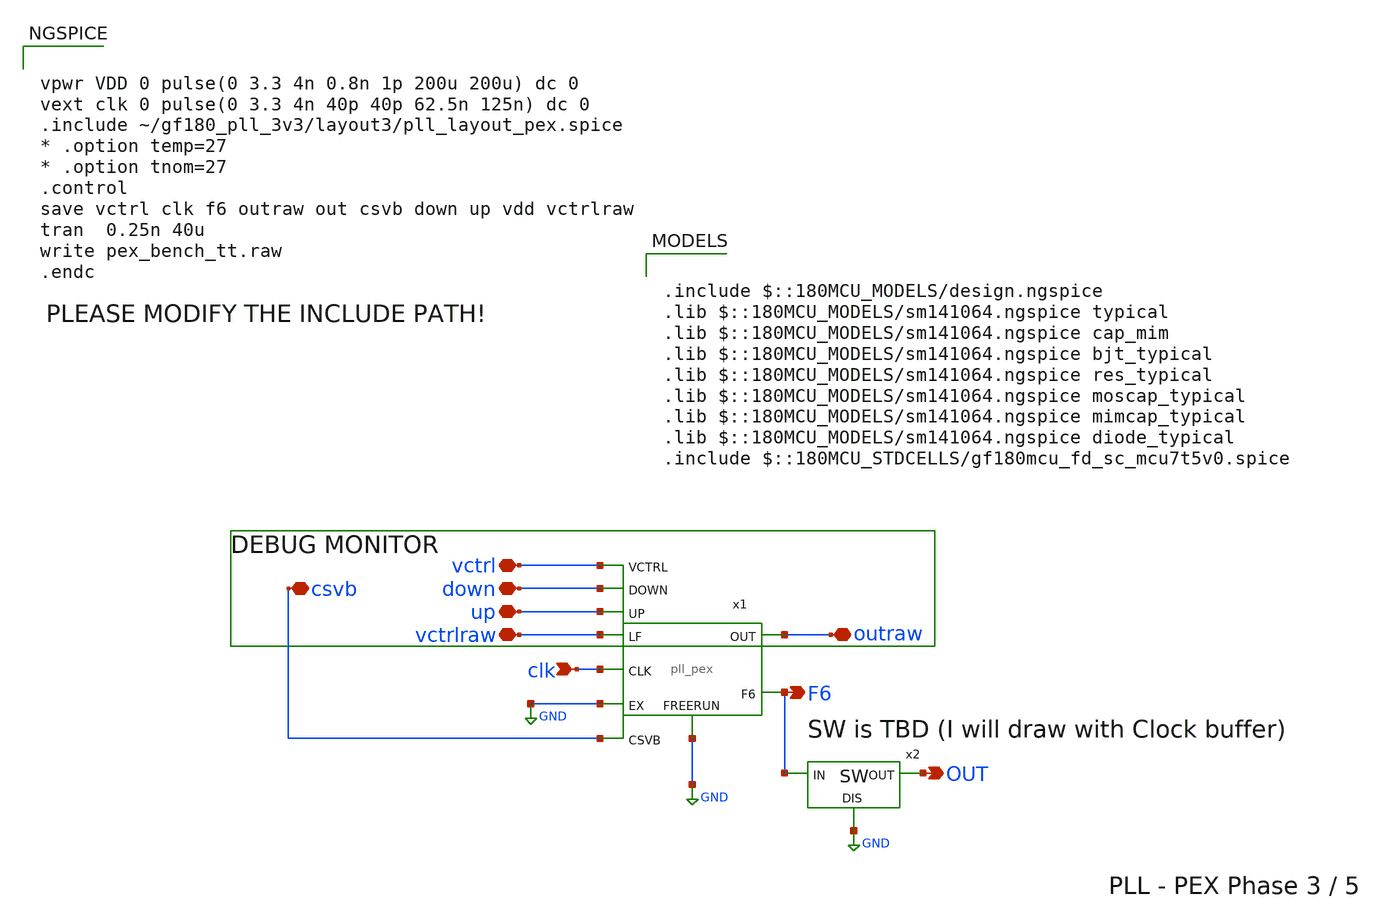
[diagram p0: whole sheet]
** sch_path: pex/pex_bench_tt.sch
**.subckt pex_bench_tt clk OUT F6 csvb up down vctrl vctrlraw outraw
*.ipin clk
*.opin OUT
*.opin F6
*.iopin csvb
*.iopin up
*.iopin down
*.iopin vctrl
*.iopin vctrlraw
*.iopin outraw
x1 up down vctrl clk VDD GND F6 0 outraw vctrlraw csvb GND TOP
x2 F6 OUT GND sw
**** begin user architecture code


vpwr VDD 0 pulse(0 3.3 4n 0.8n 1p 200u 200u) dc 0
vext clk 0 pulse(0 3.3 4n 40p 40p 62.5n 125n) dc 0
.include ~/gf180_pll_3v3/layout3/pll_layout_pex.spice
* .option temp=27
* .option tnom=27
.control
save vctrl clk f6 outraw out csvb down up vdd vctrlraw
tran  0.25n 40u
write pex_bench_tt.raw
.endc



.include $::180MCU_MODELS/design.ngspice
.lib $::180MCU_MODELS/sm141064.ngspice typical
.lib $::180MCU_MODELS/sm141064.ngspice cap_mim
.lib $::180MCU_MODELS/sm141064.ngspice bjt_typical
.lib $::180MCU_MODELS/sm141064.ngspice res_typical
.lib $::180MCU_MODELS/sm141064.ngspice moscap_typical
.lib $::180MCU_MODELS/sm141064.ngspice mimcap_typical
.lib $::180MCU_MODELS/sm141064.ngspice diode_typical
.include $::180MCU_STDCELLS/gf180mcu_fd_sc_mcu7t5v0.spice

**** end user architecture code
**.ends
.GLOBAL GND
.end
